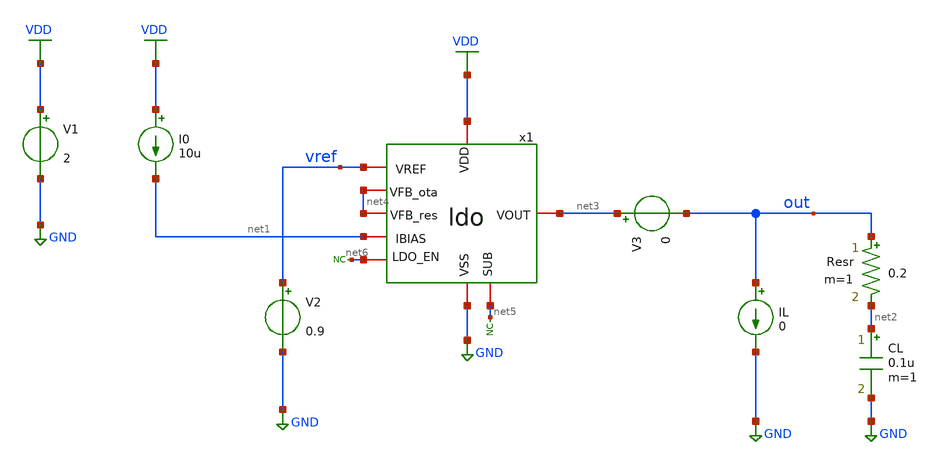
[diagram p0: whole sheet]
** sch_path: designs/libs/tb_ldo/tb_ldo/tb_ldo/tb_ldo_op/tb_ldo_op.sch
**.subckt tb_ldo_op
V1 VDD GND 2
V2 vref GND 0.9
I0 VDD net1 10u
CL net2 GND 0.1u m=1
Resr out net2 0.2 m=1
x1 VDD vref net3 net1 net5 GND net6 net4 net4 ldo
V3 net3 out 0
* noconn #net5
IL out GND 0
* noconn #net6
**** begin user architecture code

.include $::180MCU_MODELS/design.ngspice
.lib $::180MCU_MODELS/sm141064.ngspice typical
.lib $::180MCU_MODELS/sm141064.ngspice cap_mim
.lib $::180MCU_MODELS/sm141064.ngspice moscap_typical
.lib $::180MCU_MODELS/sm141064.ngspice mimcap_typical
.lib $::180MCU_MODELS/sm141064.ngspice res_typical
* .lib $::180MCU_MODELS/sm141064.ngspice res_statistical
* ngspice commands




.control
save all

** Simulations
op

** Measurements
show all
let Iload = i(V3)
let Itot = -1*i(V1)
let Iq = Itot-Iload
let Ptot = v(vdd)*Itot
let Pload = Iload*v(out)
let Pldo = Ptot-Pload
let eff = (Pload/Ptot)*100
print Itot
print Iload
print Iq
print Ptot
print Pload
print Pldo
print eff

write tb_ldo_op.raw
.endc
* ngspice commands



**** end user architecture code
**.ends
.GLOBAL GND
.GLOBAL VDD
.end
